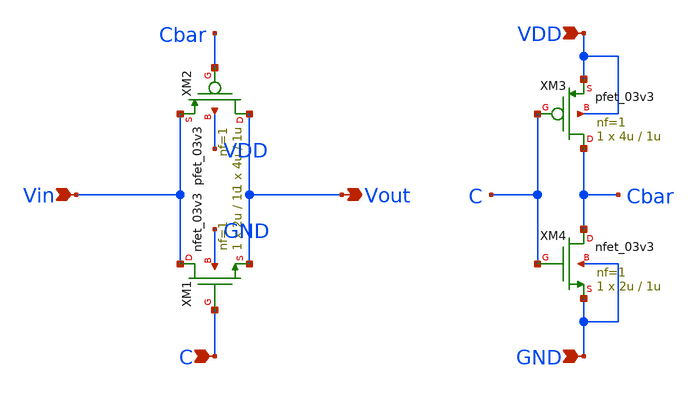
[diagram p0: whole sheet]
** sch_path: jz_trackhold/tgate_switch.sch
**.subckt tgate_switch Vout Vin GND C VDD
*.opin Vout
*.ipin Vin
*.ipin GND
*.ipin C
*.ipin VDD
XM1 Vin C Vout GND nfet_03v3 L=1u W=2u nf=1 ad='int((nf+1)/2) * W/nf * 0.18u' as='int((nf+2)/2) * W/nf * 0.18u'
+ pd='2*int((nf+1)/2) * (W/nf + 0.18u)' ps='2*int((nf+2)/2) * (W/nf + 0.18u)' nrd='0.18u / W' nrs='0.18u / W'
+ sa=0 sb=0 sd=0 m=1
XM2 Vout Cbar Vin VDD pfet_03v3 L=1u W=4u nf=1 ad='int((nf+1)/2) * W/nf * 0.18u' as='int((nf+2)/2) * W/nf * 0.18u'
+ pd='2*int((nf+1)/2) * (W/nf + 0.18u)' ps='2*int((nf+2)/2) * (W/nf + 0.18u)' nrd='0.18u / W' nrs='0.18u / W'
+ sa=0 sb=0 sd=0 m=1
XM3 Cbar C VDD VDD pfet_03v3 L=1u W=4u nf=1 ad='int((nf+1)/2) * W/nf * 0.18u' as='int((nf+2)/2) * W/nf * 0.18u'
+ pd='2*int((nf+1)/2) * (W/nf + 0.18u)' ps='2*int((nf+2)/2) * (W/nf + 0.18u)' nrd='0.18u / W' nrs='0.18u / W'
+ sa=0 sb=0 sd=0 m=1
XM4 Cbar C GND GND nfet_03v3 L=1u W=2u nf=1 ad='int((nf+1)/2) * W/nf * 0.18u' as='int((nf+2)/2) * W/nf * 0.18u'
+ pd='2*int((nf+1)/2) * (W/nf + 0.18u)' ps='2*int((nf+2)/2) * (W/nf + 0.18u)' nrd='0.18u / W' nrs='0.18u / W'
+ sa=0 sb=0 sd=0 m=1
**.ends
.end
